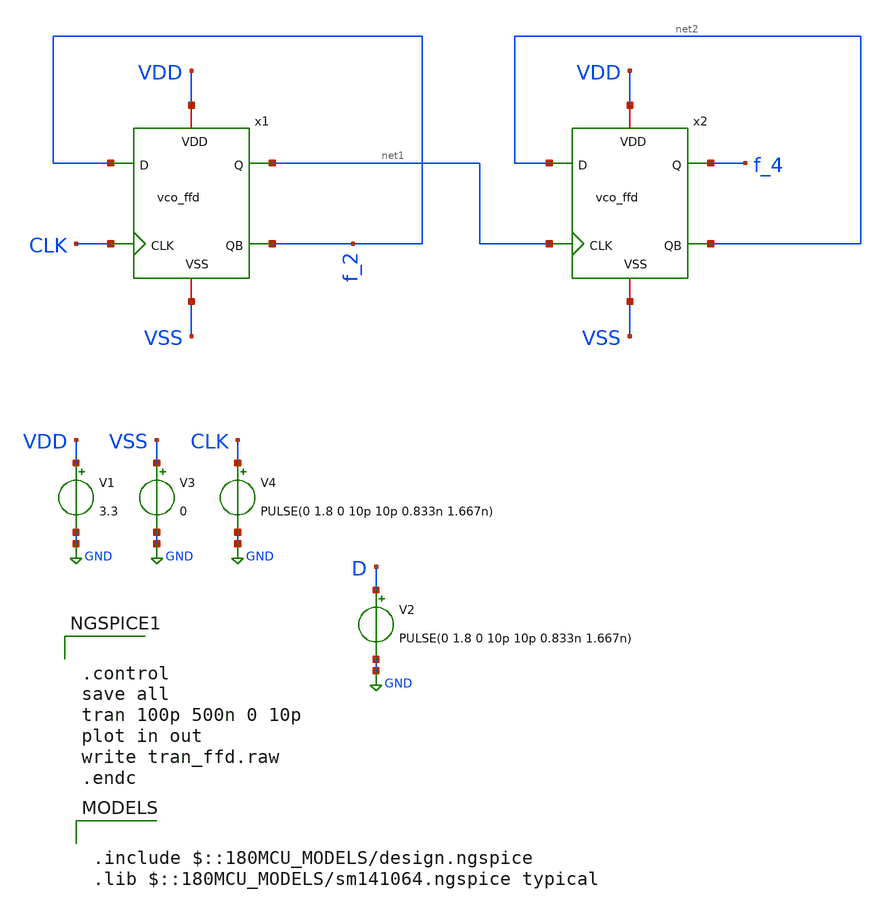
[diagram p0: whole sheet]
** sch_path: designs/untitled-1.sch
**.subckt untitled-1
V1 VDD GND 3.3
V3 VSS GND 0
V4 CLK GND PULSE(0 1.8 0 10p 10p 0.833n 1.667n)
V2 D GND PULSE(0 1.8 0 10p 10p 0.833n 1.667n)
x1 VSS VDD f_2 CLK net1 f_2 vco_ffd
x2 VSS VDD net2 net1 f_4 net2 vco_ffd
**** begin user architecture code

.include $::180MCU_MODELS/design.ngspice
.lib $::180MCU_MODELS/sm141064.ngspice typical



.control
save all
tran 100p 500n 0 10p
plot in out
write tran_ffd.raw
.endc


**** end user architecture code
**.ends

* expanding   symbol:  libs/core_vco/vco_ffd/vco_ffd.sym # of pins=6
** sym_path: designs/libs/core_vco/vco_ffd/vco_ffd.sym
** sch_path: designs/libs/core_vco/vco_ffd/vco_ffd.sch
.subckt vco_ffd VSS VDD D CLK Q QB
*.opin Q
*.iopin VSS
*.ipin D
*.iopin VDD
*.ipin CLK
*.opin QB
XM5 Q net1 VSS VSS nfet_03v3 L=0.28u W=1u nf=1 ad='int((nf+1)/2) * W/nf * 0.18u' as='int((nf+2)/2) * W/nf * 0.18u'
+ pd='2*int((nf+1)/2) * (W/nf + 0.18u)' ps='2*int((nf+2)/2) * (W/nf + 0.18u)' nrd='0.18u / W' nrs='0.18u / W'
+ sa=0 sb=0 sd=0 m=1
XM6 Q net1 VDD VDD pfet_03v3 L=0.28u W=1u nf=2 ad='int((nf+1)/2) * W/nf * 0.18u' as='int((nf+2)/2) * W/nf * 0.18u'
+ pd='2*int((nf+1)/2) * (W/nf + 0.18u)' ps='2*int((nf+2)/2) * (W/nf + 0.18u)' nrd='0.18u / W' nrs='0.18u / W'
+ sa=0 sb=0 sd=0 m=1
XM1 QB Q VSS VSS nfet_03v3 L=0.28u W=1u nf=1 ad='int((nf+1)/2) * W/nf * 0.18u' as='int((nf+2)/2) * W/nf * 0.18u'
+ pd='2*int((nf+1)/2) * (W/nf + 0.18u)' ps='2*int((nf+2)/2) * (W/nf + 0.18u)' nrd='0.18u / W' nrs='0.18u / W'
+ sa=0 sb=0 sd=0 m=1
XM2 QB Q VDD VDD pfet_03v3 L=0.28u W=1u nf=2 ad='int((nf+1)/2) * W/nf * 0.18u' as='int((nf+2)/2) * W/nf * 0.18u'
+ pd='2*int((nf+1)/2) * (W/nf + 0.18u)' ps='2*int((nf+2)/2) * (W/nf + 0.18u)' nrd='0.18u / W' nrs='0.18u / W'
+ sa=0 sb=0 sd=0 m=1
XM3 net1 net3 VDD VDD pfet_03v3 L=0.28u W=1.2u nf=2 ad='int((nf+1)/2) * W/nf * 0.18u' as='int((nf+2)/2) * W/nf * 0.18u'
+ pd='2*int((nf+1)/2) * (W/nf + 0.18u)' ps='2*int((nf+2)/2) * (W/nf + 0.18u)' nrd='0.18u / W' nrs='0.18u / W'
+ sa=0 sb=0 sd=0 m=1
XM7 net2 net3 VSS VSS nfet_03v3 L=0.28u W=1.2u nf=1 ad='int((nf+1)/2) * W/nf * 0.18u' as='int((nf+2)/2) * W/nf * 0.18u'
+ pd='2*int((nf+1)/2) * (W/nf + 0.18u)' ps='2*int((nf+2)/2) * (W/nf + 0.18u)' nrd='0.18u / W' nrs='0.18u / W'
+ sa=0 sb=0 sd=0 m=1
XM8 net3 CLK VDD VDD pfet_03v3 L=0.28u W=0.5u nf=2 ad='int((nf+1)/2) * W/nf * 0.18u' as='int((nf+2)/2) * W/nf * 0.18u'
+ pd='2*int((nf+1)/2) * (W/nf + 0.18u)' ps='2*int((nf+2)/2) * (W/nf + 0.18u)' nrd='0.18u / W' nrs='0.18u / W'
+ sa=0 sb=0 sd=0 m=1
XM10 net4 CLK VSS VSS nfet_03v3 L=0.28u W=0.5u nf=1 ad='int((nf+1)/2) * W/nf * 0.18u' as='int((nf+2)/2) * W/nf * 0.18u'
+ pd='2*int((nf+1)/2) * (W/nf + 0.18u)' ps='2*int((nf+2)/2) * (W/nf + 0.18u)' nrd='0.18u / W' nrs='0.18u / W'
+ sa=0 sb=0 sd=0 m=1
XM11 net5 D VDD VDD pfet_03v3 L=0.28u W=1.2u nf=2 ad='int((nf+1)/2) * W/nf * 0.18u' as='int((nf+2)/2) * W/nf * 0.18u'
+ pd='2*int((nf+1)/2) * (W/nf + 0.18u)' ps='2*int((nf+2)/2) * (W/nf + 0.18u)' nrd='0.18u / W' nrs='0.18u / W'
+ sa=0 sb=0 sd=0 m=1
XM12 net6 CLK net5 VDD pfet_03v3 L=0.28u W=0.5u nf=2 ad='int((nf+1)/2) * W/nf * 0.18u' as='int((nf+2)/2) * W/nf * 0.18u'
+ pd='2*int((nf+1)/2) * (W/nf + 0.18u)' ps='2*int((nf+2)/2) * (W/nf + 0.18u)' nrd='0.18u / W' nrs='0.18u / W'
+ sa=0 sb=0 sd=0 m=1
XM13 net6 D VSS VSS nfet_03v3 L=0.28u W=1.2u nf=1 ad='int((nf+1)/2) * W/nf * 0.18u' as='int((nf+2)/2) * W/nf * 0.18u'
+ pd='2*int((nf+1)/2) * (W/nf + 0.18u)' ps='2*int((nf+2)/2) * (W/nf + 0.18u)' nrd='0.18u / W' nrs='0.18u / W'
+ sa=0 sb=0 sd=0 m=1
XM14 net3 net6 net4 VSS nfet_03v3 L=0.28u W=1.2u nf=1 ad='int((nf+1)/2) * W/nf * 0.18u' as='int((nf+2)/2) * W/nf * 0.18u'
+ pd='2*int((nf+1)/2) * (W/nf + 0.18u)' ps='2*int((nf+2)/2) * (W/nf + 0.18u)' nrd='0.18u / W' nrs='0.18u / W'
+ sa=0 sb=0 sd=0 m=1
XM4 net1 CLK net2 VSS nfet_03v3 L=0.28u W=0.5u nf=1 ad='int((nf+1)/2) * W/nf * 0.18u' as='int((nf+2)/2) * W/nf * 0.18u'
+ pd='2*int((nf+1)/2) * (W/nf + 0.18u)' ps='2*int((nf+2)/2) * (W/nf + 0.18u)' nrd='0.18u / W' nrs='0.18u / W'
+ sa=0 sb=0 sd=0 m=1
.ends

.GLOBAL GND
.end
